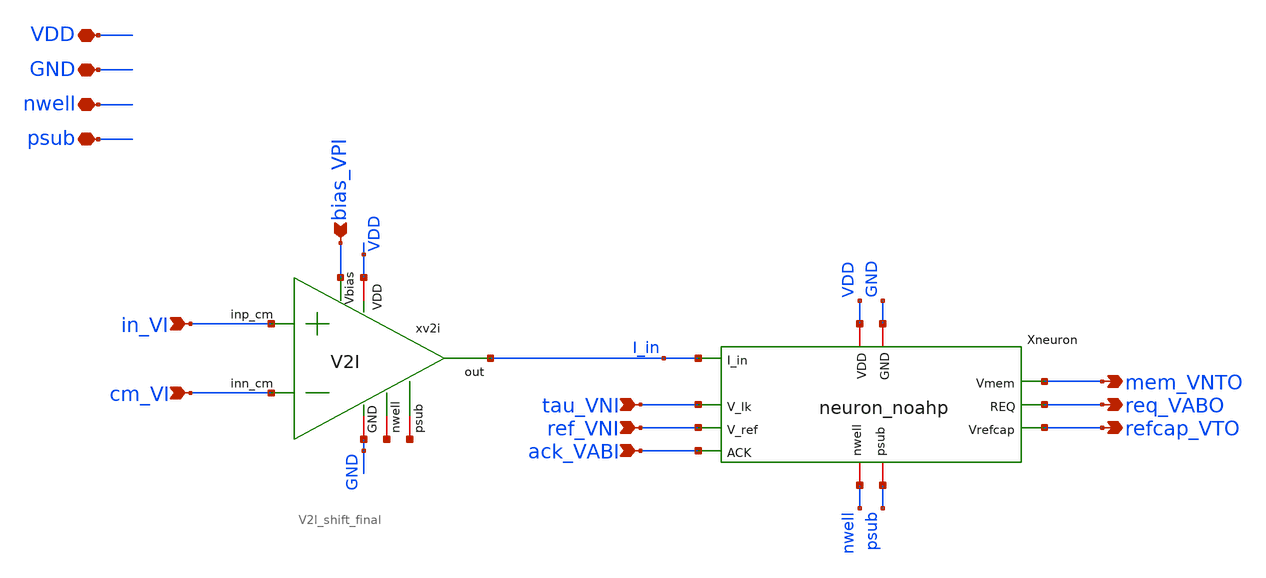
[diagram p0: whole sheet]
** sch_path: xschem/neuron_row.sch
**.subckt neuron_row in_VI cm_VI bias_VPI VDD GND nwell psub mem_VNTO req_VABO refcap_VTO tau_VNI
*+ ref_VNI ack_VABI
*.ipin in_VI
*.ipin cm_VI
*.ipin bias_VPI
*.iopin VDD
*.iopin GND
*.iopin nwell
*.iopin psub
*.opin mem_VNTO
*.opin req_VABO
*.opin refcap_VTO
*.ipin tau_VNI
*.ipin ref_VNI
*.ipin ack_VABI
Xneuron VDD I_in tau_VNI mem_VNTO req_VABO ack_VABI ref_VNI GND refcap_VTO psub nwell neuron_noahp
xv2i VDD bias_VPI cm_VI in_VI I_in GND net1 net2 V2I_shift_final
**.ends
.end
